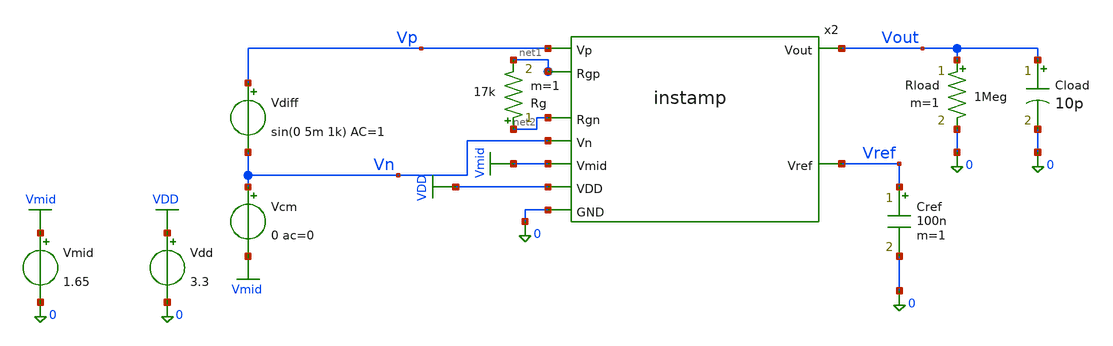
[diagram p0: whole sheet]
** sch_path: xschem/instamp_tb.sch
* Copyright 2021 Stefan Frederik Schippers
* Licensed under the Apache License, Version 2.0 (the "License");
* you may not use this file except in compliance with the License.
* You may obtain a copy of the License at
* https://www.apache.org/licenses/LICENSE-2.0
* Unless required by applicable law or agreed to in writing, software
* distributed under the License is distributed on an "AS IS" BASIS,
* WITHOUT WARRANTIES OR CONDITIONS OF ANY KIND, either express or implied.
* See the License for the specific language governing permissions and
* limitations under the License.
**.subckt instamp_tb
Vdd VDD 0 3.3
Vdiff Vp Vn sin(0 5m 1k) AC=1
Vmid Vmid 0 1.65
Vcm Vn Vmid 0 ac=0
x2 Vn net2 Vp net1 Vmid Vout Vref VDD 0 instamp
Cref Vref 0 100n m=1
Rg net2 net1 17k m=1
Rload Vout 0 1Meg m=1
Cload Vout 0 10p m=1
**** begin user architecture code

** opencircuitdesign pdks install
.lib $::SKYWATER_MODELS/sky130.lib.spice tt



.option wnflag=1
.option savecurrents
#.option rshunt=1e12

# if one of these is uncommented, it will
# override the subcircuit in the symbol
# from the cace extracction
.include ../netlist/rcx/instamp.spice
# from the mag extraction
#.include ../netlist/layout/instamp.spice

.save all
.control
if 0
op
write instamp_tb.raw
endif

set appendwrite
set gnuplot_terminal=png/quit

* write instamp_tb.raw
if 0
* differential gain tran
  destroy all
  foreach val 10k 5k 1k
    alter Rg = $val
    tran 10u 3m 1m
  end
  let Rg10k = tran1.v(vout)
  let Rg5k = tran2.v(vout)
  let Rg1k = tran3.v(vout)
  gnuplot tran Rg10k Rg5k Rg1k
*+ title 'Differential gain'  xlabel 'Time' ylabel 'Volts'
endif

# rise and fall times
if 0
let per=5u
let tstop=$&per*3
let tstep=per/1000
alter Rg=90k
alter @Vdiff[pulse] [ 0 100m $&per 1n 1n $&per $&tstop ]
tran $&tstep $&tstop
plot V(Vp,vmid) V(vout,vmid)
meas tran v_min MIN V(Vout)
meas tran v_pp PP V(Vout)
let v_high=(0.9*v_pp)+v_min
let v_low=(0.1*v_pp)+v_min
meas tran rise_time TRIG v(Vout) VAL='v_low' rise=1 targ v(vout) Val='v_high' RISE=1
let sr=(v_high-v_low)/rise_time
print sr

  gnuplot v_rise_fall V(vp,vmid) V(Vout,vmid)  title 'Rise and Fall Times'  xlabel 'Time (s)' ylabel
+ 'Volts'

endif

if 0
ac dec 100 1 1Meg
let gain = db(V(Vout))
let cutoff_db = vecmax(gain)-3.0
meas ac bw WHEN gain=cutoff_db FALL =1
meas ac max_gain MAX gain
print bw max_gain
endif
* run ac on schematic as drawn
if 1
  destroy all
* differential gain ac
  ac dec 100 1 1Meg
  plot db(v(vout))
endif

* run ac cmrr and psrr sweeps
if 0
  destroy all
* differential gain ac
  alter vdiff ac=1
  alter vcm ac=0
  alter vdd ac=0
  foreach val 10k 5k 1k
    alter Rg = $val
    ac dec 100 1 1Meg
  end
  alter vdiff ac=0
  alter vcm ac=1
  alter vdd ac=0
  foreach val 10k 5k 1k
    alter Rg = $val
    ac dec 100 1 1Meg
  end
  alter vdiff ac=0
  alter vcm ac=0
  alter vdd ac=1
  foreach val 10k 5k 1k
    alter Rg = $val
    ac dec 100 1 1Meg
  end
  alter vdiff ac=0
  alter vcm ac=0
  alter vdd ac=0
  alter vmid ac=1
  foreach val 10k 5k 1k
    alter Rg = $val
    ac dec 100 1 1Meg
  end
  let Rg10k = db(ac1.v(vout))
  let Rg5k = db(ac2.v(vout))
  let Rg1k = db(ac3.v(vout))
  let Rg10k_cm = Rg10k-db(ac4.v(vout))
  let Rg5k_cm = Rg5k-db(ac5.v(vout))
  let Rg1k_cm = Rg1k-db(ac6.v(vout))
  let Rg10k_psh = Rg10k-db(ac7.v(vout))
  let Rg5k_psh = Rg5k-db(ac8.v(vout))
  let Rg1k_psh = Rg1k-db(ac9.v(vout))
  let Rg10k_vmid = Rg10k-db(ac10.v(vout))
  let Rg5k_vmid = Rg5k-db(ac11.v(vout))
  let Rg1k_vmid = Rg1k-db(ac12.v(vout))

  gnuplot ac Rg10k Rg5k Rg1k  title 'Differential gain'  xlabel 'Freq' ylabel 'Gain dB'
  gnuplot cmrr Rg10k_cm Rg5k_cm Rg1k_cm  title 'CMRR'  xlabel 'Freq' ylabel 'Gain dB'
  gnuplot psrr Rg10k_psh Rg5k_psh Rg1k_psh  title 'PSRR'  xlabel 'Freq' ylabel 'Gain dB'
  gnuplot vmid_rej Rg10k_vmid Rg5k_vmid Rg1k_vmid  title 'Vmid Rejection'  xlabel 'Freq' ylabel 'Gain dB'

endif

if 0
* common mode gain
  alter vdiff ac=0
  alter vcm ac=1
  foreach val 90k 5k 1k
    alter Rg = $val
    ac dec 100 1 10Meg
  end

  plot db(ac1.V(Vout)) db(ac2.V(Vout))   db(ac3.V(Vout)) title 'Mag Vout'

* power supply gain
  alter vcm ac=0
  alter vdd ac=1
  foreach val 90k 5k 1k
    alter Rg = $val
    ac dec 100 1 10Meg
  end

  plot db(ac4.V(Vout)) db(ac5.V(Vout))   db(ac6.V(Vout)) title 'Mag Vout'

endif

.endc


**** end user architecture code
**.ends
.GLOBAL VDD
.GLOBAL Vmid
.end
